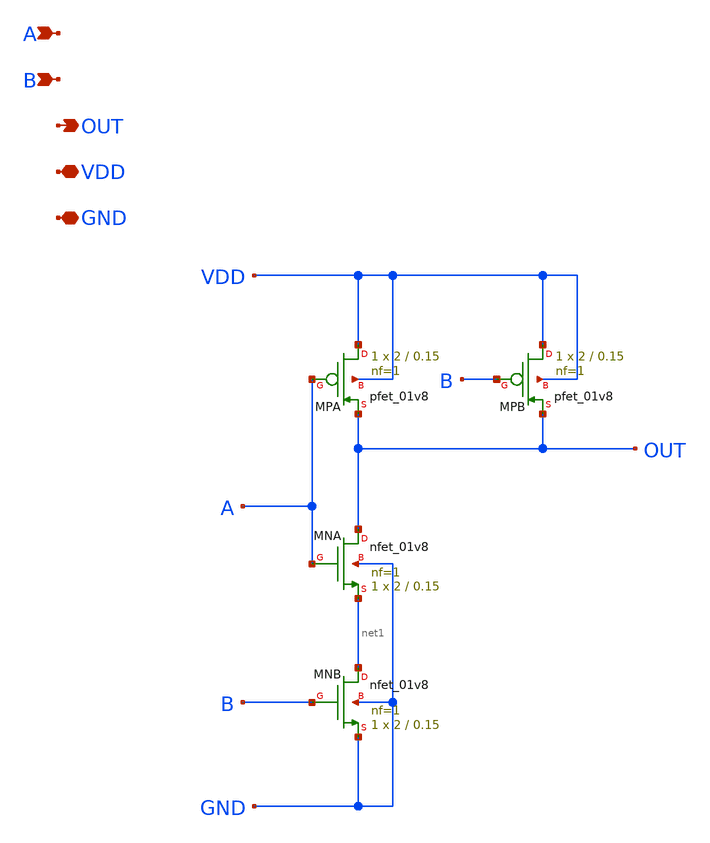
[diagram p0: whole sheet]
** sch_path: blocks/06_Clock_gen/xschem/B6_NAND2.sch
**.subckt B6_NAND2 A B OUT VDD GND
*.ipin A
*.ipin B
*.opin OUT
*.iopin VDD
*.iopin GND
XMPA VDD A OUT VDD sky130_fd_pr__pfet_01v8 L=0.15 W=2 nf=1 ad='int((1 + 1)/2) * 2 / 1 * 0.29' as='int((1 + 2)/2) * 2 / 1 * 0.29'
+ pd='2*int((1 + 1)/2) * (2 / 1 + 0.29)' ps='2*int((1 + 2)/2) * (2 / 1 + 0.29)' nrd='0.29 / 2 ' nrs='0.29 / 2 '
+ sa=0 sb=0 sd=0 mult=1 m=1
XMPB VDD B OUT VDD sky130_fd_pr__pfet_01v8 L=0.15 W=2 nf=1 ad='int((1 + 1)/2) * 2 / 1 * 0.29' as='int((1 + 2)/2) * 2 / 1 * 0.29'
+ pd='2*int((1 + 1)/2) * (2 / 1 + 0.29)' ps='2*int((1 + 2)/2) * (2 / 1 + 0.29)' nrd='0.29 / 2 ' nrs='0.29 / 2 '
+ sa=0 sb=0 sd=0 mult=1 m=1
XMNA OUT A net1 GND sky130_fd_pr__nfet_01v8 L=0.15 W=2 nf=1 ad='int((1 + 1)/2) * 2 / 1 * 0.29' as='int((1 + 2)/2) * 2 / 1 * 0.29'
+ pd='2*int((1 + 1)/2) * (2 / 1 + 0.29)' ps='2*int((1 + 2)/2) * (2 / 1 + 0.29)' nrd='0.29 / 2 ' nrs='0.29 / 2 '
+ sa=0 sb=0 sd=0 mult=1 m=1
XMNB net1 B GND GND sky130_fd_pr__nfet_01v8 L=0.15 W=2 nf=1 ad='int((1 + 1)/2) * 2 / 1 * 0.29' as='int((1 + 2)/2) * 2 / 1 * 0.29'
+ pd='2*int((1 + 1)/2) * (2 / 1 + 0.29)' ps='2*int((1 + 2)/2) * (2 / 1 + 0.29)' nrd='0.29 / 2 ' nrs='0.29 / 2 '
+ sa=0 sb=0 sd=0 mult=1 m=1
**.ends
.end
